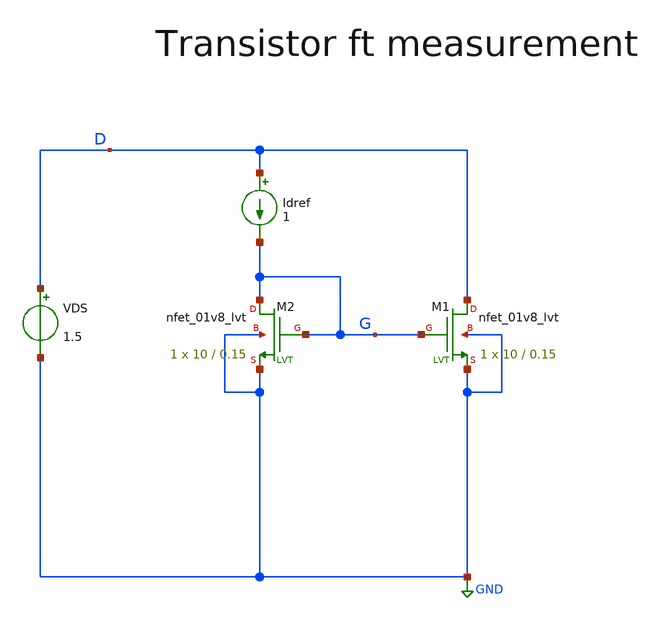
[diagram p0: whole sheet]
** sch_path: xyce/sky130A-xyce/libs.tech/xschem/sky130_tests/tb_ft_test.sch
**.subckt tb_ft_test
XM1 D G GND GND sky130_fd_pr__nfet_01v8_lvt L=0.15 W=10 nf=1 ad='int((nf+1)/2) * W/nf * 0.29' as='int((nf+2)/2) * W/nf * 0.29'
+ pd='2*int((nf+1)/2) * (W/nf + 0.29)' ps='2*int((nf+2)/2) * (W/nf + 0.29)' nrd='0.29 / W' nrs='0.29 / W'
+ sa=0 sb=0 sd=0 mult=1 m=1
VDS D GND 1.5
Idref D G 1
XM2 G G GND GND sky130_fd_pr__nfet_01v8_lvt L=0.15 W=10 nf=1 ad='int((nf+1)/2) * W/nf * 0.29' as='int((nf+2)/2) * W/nf * 0.29'
+ pd='2*int((nf+1)/2) * (W/nf + 0.29)' ps='2*int((nf+2)/2) * (W/nf + 0.29)' nrd='0.29 / W' nrs='0.29 / W'
+ sa=0 sb=0 sd=0 mult=1 m=1
**** begin user architecture code



.options filetype=ascii
.save all

.op
.control
*dc Idref 0.1e-3 10e-3 0.1e-3

let n_idx = 101

let start_iref = 0.1e-3
let stop_iref = 10e-3
let delta_iref = (stop_iref - start_iref) / n_idx
let iref_act = start_iref

let vgs = unitvec(n_idx)
let gms = unitvec(n_idx)
let ids = unitvec(n_idx)

let cgss = unitvec(n_idx)
let cgds = unitvec(n_idx)

let idxs = 0
let idx = idxs

*loop
while iref_act le stop_iref
  alter idref iref_act
  run
  *print @m.xm2.msky130_fd_pr__nfet_01v8_lvt[gm]

  let gms[idx] = @m.xm2.msky130_fd_pr__nfet_01v8_lvt[gm]
  let ids[idx] = @m.xm2.msky130_fd_pr__nfet_01v8_lvt[id]

  let cgss[idx] = @m.xm2.msky130_fd_pr__nfet_01v8_lvt[cgs]
  let cgds[idx] = @m.xm2.msky130_fd_pr__nfet_01v8_lvt[cgd]
  let vgs[idx] = v(G)

  let iref_act = iref_act + delta_iref
  let idxs = idx + 1
  let idx = idxs
end

let ft = -gms/(2*pi*(cgss+cgds))
settype voltage vgs
settype current ids
setscale ids
plot gms vs ids
plot xlog ft vs ids
plot xlog vgs vs ids

.endc
.end



.include $::SKYWATER_MODELS/cells/nfet_01v8/sky130_fd_pr__nfet_01v8__tt.corner.spice
.include $::SKYWATER_MODELS/cells/nfet_01v8_lvt/sky130_fd_pr__nfet_01v8_lvt__tt.corner.spice
.include $::SKYWATER_MODELS/cells/pfet_01v8/sky130_fd_pr__pfet_01v8__tt.corner.spice
.include $::SKYWATER_MODELS/cells/nfet_03v3_nvt/sky130_fd_pr__nfet_03v3_nvt__tt.corner.spice
.include $::SKYWATER_MODELS/cells/nfet_05v0_nvt/sky130_fd_pr__nfet_05v0_nvt__tt.corner.spice
.include $::SKYWATER_MODELS/cells/esd_nfet_01v8/sky130_fd_pr__esd_nfet_01v8__tt.corner.spice
.include $::SKYWATER_MODELS/cells/pfet_01v8_lvt/sky130_fd_pr__pfet_01v8_lvt__tt.corner.spice
.include $::SKYWATER_MODELS/cells/pfet_01v8_hvt/sky130_fd_pr__pfet_01v8_hvt__tt.corner.spice
.include $::SKYWATER_MODELS/cells/esd_pfet_g5v0d10v5/sky130_fd_pr__esd_pfet_g5v0d10v5__tt.corner.spice
.include $::SKYWATER_MODELS/cells/pfet_g5v0d10v5/sky130_fd_pr__pfet_g5v0d10v5__tt.corner.spice
.include $::SKYWATER_MODELS/cells/pfet_g5v0d16v0/sky130_fd_pr__pfet_g5v0d16v0__tt.corner.spice
.include $::SKYWATER_MODELS/cells/nfet_g5v0d10v5/sky130_fd_pr__nfet_g5v0d10v5__tt.corner.spice
.include $::SKYWATER_MODELS/cells/nfet_g5v0d16v0/sky130_fd_pr__nfet_g5v0d16v0__tt_discrete.corner.spice
.include $::SKYWATER_MODELS/cells/esd_nfet_g5v0d10v5/sky130_fd_pr__esd_nfet_g5v0d10v5__tt.corner.spice
.include $::SKYWATER_MODELS/models/corners/tt/nonfet.spice
* Mismatch parameters
.include $::SKYWATER_MODELS/cells/nfet_01v8/sky130_fd_pr__nfet_01v8__mismatch.corner.spice
.include $::SKYWATER_MODELS/cells/pfet_01v8/sky130_fd_pr__pfet_01v8__mismatch.corner.spice
.include $::SKYWATER_MODELS/cells/nfet_01v8_lvt/sky130_fd_pr__nfet_01v8_lvt__mismatch.corner.spice
.include $::SKYWATER_MODELS/cells/pfet_01v8_lvt/sky130_fd_pr__pfet_01v8_lvt__mismatch.corner.spice
.include $::SKYWATER_MODELS/cells/pfet_01v8_hvt/sky130_fd_pr__pfet_01v8_hvt__mismatch.corner.spice
.include $::SKYWATER_MODELS/cells/nfet_g5v0d10v5/sky130_fd_pr__nfet_g5v0d10v5__mismatch.corner.spice
.include $::SKYWATER_MODELS/cells/pfet_g5v0d10v5/sky130_fd_pr__pfet_g5v0d10v5__mismatch.corner.spice
.include $::SKYWATER_MODELS/cells/nfet_05v0_nvt/sky130_fd_pr__nfet_05v0_nvt__mismatch.corner.spice
.include $::SKYWATER_MODELS/cells/nfet_03v3_nvt/sky130_fd_pr__nfet_03v3_nvt__mismatch.corner.spice
* Resistor$::SKYWATER_MODELS/Capacitor
.include $::SKYWATER_MODELS/models/r+c/res_typical__cap_typical.spice
.include $::SKYWATER_MODELS/models/r+c/res_typical__cap_typical__lin.spice
* Special cells
.include $::SKYWATER_MODELS/models/corners/tt/specialized_cells.spice
* All models
.include $::SKYWATER_MODELS/models/all.spice
* Corner
.include $::SKYWATER_MODELS/models/corners/tt/rf.spice

**** end user architecture code
**.ends
.GLOBAL GND
.end
